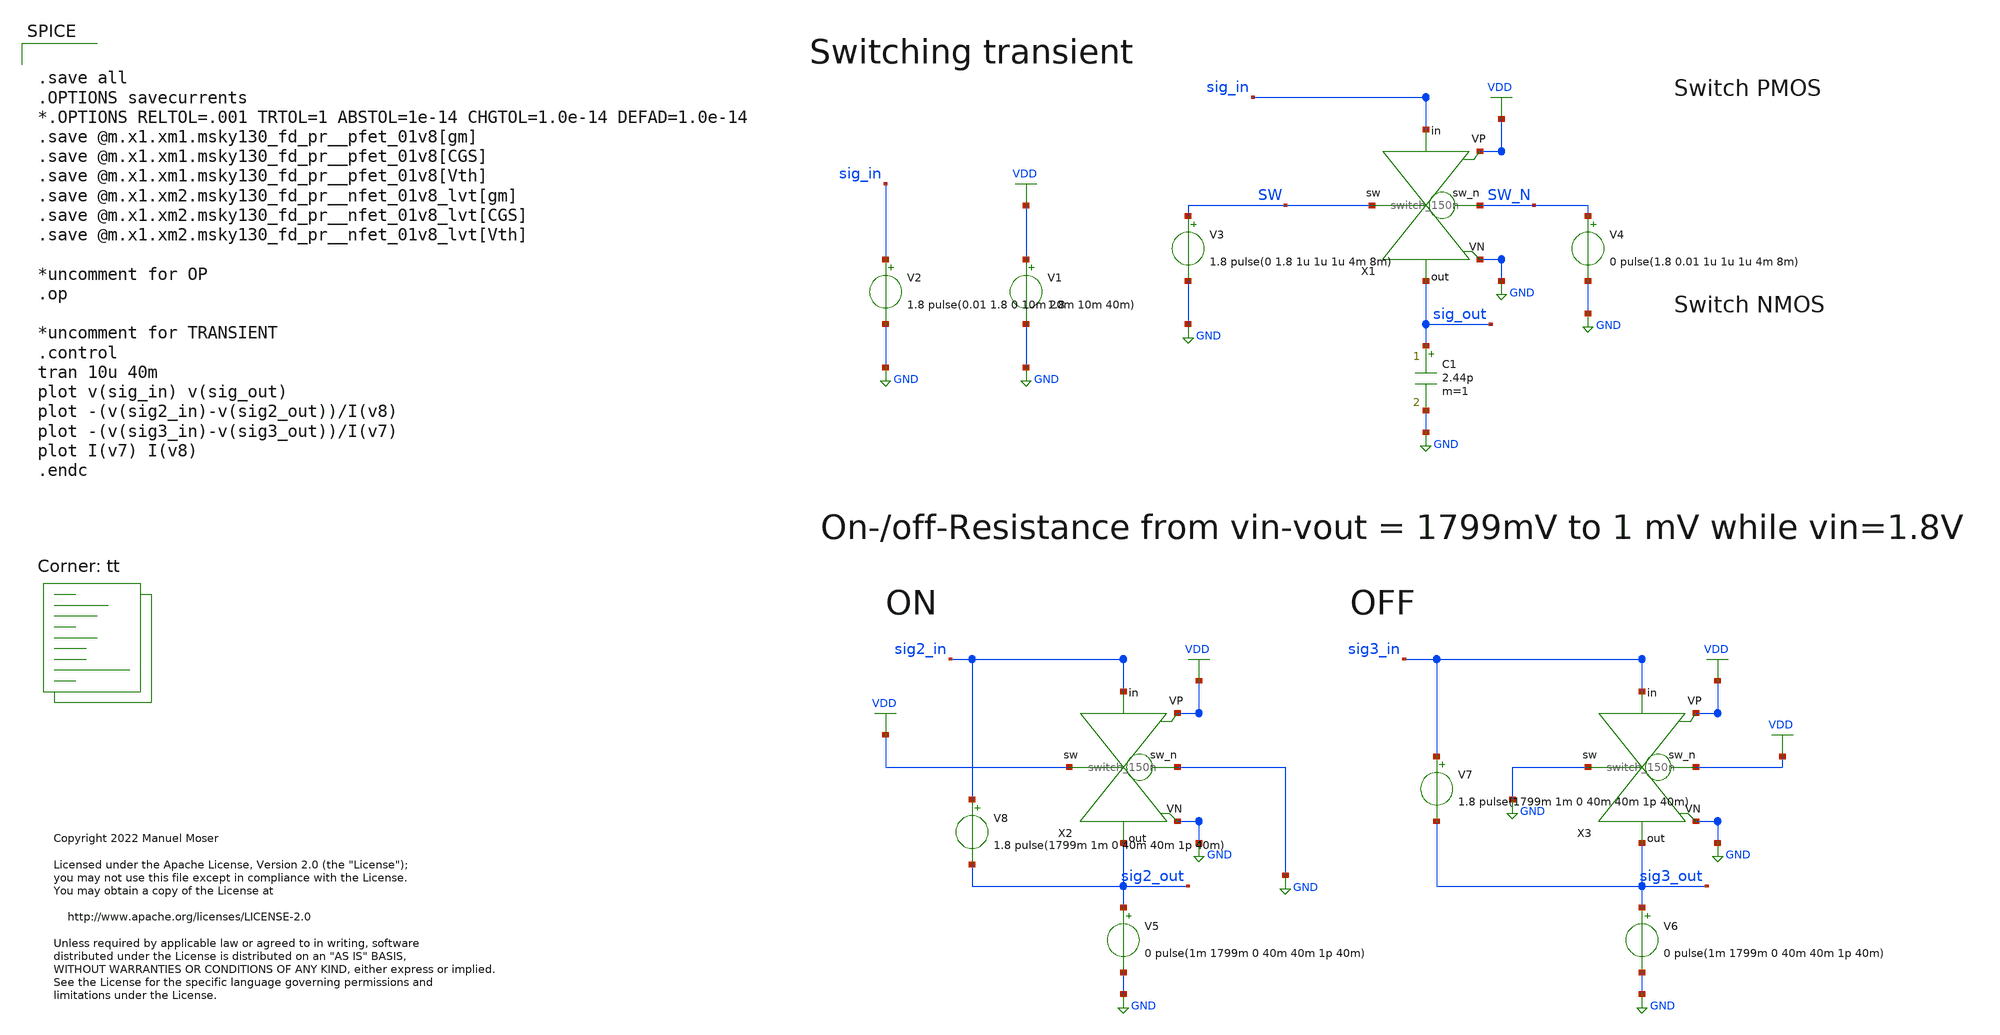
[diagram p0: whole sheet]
** sch_path: xschem/switch/switch_150n_tb.sch
* Copyright 2022 Manuel Moser
* Licensed under the Apache License, Version 2.0 (the "License");
**.subckt switch_150n_tb
V1 VDD GND 1.8
V2 sig_in GND 1.8 pulse(0.01 1.8 0 10m 20m 10m 40m)
V3 SW GND 1.8 pulse(0 1.8 1u 1u 1u 4m 8m)
V4 SW_N GND 0 pulse(1.8 0.01 1u 1u 1u 4m 8m)
X1 SW_N sig_in SW sig_out VDD GND switch_150n
C1 sig_out GND 2.44p m=1
X2 GND sig2_in VDD sig2_out VDD GND switch_150n
V5 sig2_out GND 0 pulse(1m 1799m 0 40m 40m 1p 40m)
X3 VDD sig3_in GND sig3_out VDD GND switch_150n
V6 sig3_out GND 0 pulse(1m 1799m 0 40m 40m 1p 40m)
V7 sig3_in sig3_out 1.8 pulse(1799m 1m 0 40m 40m 1p 40m)
V8 sig2_in sig2_out 1.8 pulse(1799m 1m 0 40m 40m 1p 40m)
**** begin user architecture code


.save all
.OPTIONS savecurrents
*.OPTIONS RELTOL=.001 TRTOL=1 ABSTOL=1e-14 CHGTOL=1.0e-14 DEFAD=1.0e-14
.save @m.x1.xm1.msky130_fd_pr__pfet_01v8[gm]
.save @m.x1.xm1.msky130_fd_pr__pfet_01v8[CGS]
.save @m.x1.xm1.msky130_fd_pr__pfet_01v8[Vth]
.save @m.x1.xm2.msky130_fd_pr__nfet_01v8_lvt[gm]
.save @m.x1.xm2.msky130_fd_pr__nfet_01v8_lvt[CGS]
.save @m.x1.xm2.msky130_fd_pr__nfet_01v8_lvt[Vth]

*uncomment for OP
.op

*uncomment for TRANSIENT
.control
tran 10u 40m
plot v(sig_in) v(sig_out)
plot -(v(sig2_in)-v(sig2_out))/I(v8)
plot -(v(sig3_in)-v(sig3_out))/I(v7)
plot I(v7) I(v8)
.endc


.lib $::SKYWATER_MODELS/sky130.lib.spice tt
**** end user architecture code
**.ends

* expanding   symbol:  switch_150n.sym # of pins=6
** sym_path: xschem/switch/switch_150n.sym
** sch_path: xschem/switch/switch_150n.sch
.subckt switch_150n sw_n in sw out VP VN
*.iopin VN
*.iopin VP
*.ipin IN
*.opin OUT
*.ipin SW_N
*.ipin SW
XM2 IN SW OUT VN sky130_fd_pr__nfet_01v8_lvt L=0.35 W=2 nf=1 ad='int((nf+1)/2) * W/nf * 0.29' as='int((nf+2)/2) * W/nf * 0.29'
+ pd='2*int((nf+1)/2) * (W/nf + 0.29)' ps='2*int((nf+2)/2) * (W/nf + 0.29)' nrd='0.29 / W' nrs='0.29 / W'
+ sa=0 sb=0 sd=0 mult=1 m=1
XM1 IN SW_N OUT VP sky130_fd_pr__pfet_01v8 L=0.15 W=1.7 nf=1 ad='int((nf+1)/2) * W/nf * 0.29' as='int((nf+2)/2) * W/nf * 0.29'
+ pd='2*int((nf+1)/2) * (W/nf + 0.29)' ps='2*int((nf+2)/2) * (W/nf + 0.29)' nrd='0.29 / W' nrs='0.29 / W'
+ sa=0 sb=0 sd=0 mult=1 m=1
.ends

.GLOBAL GND
.GLOBAL VDD
.end
